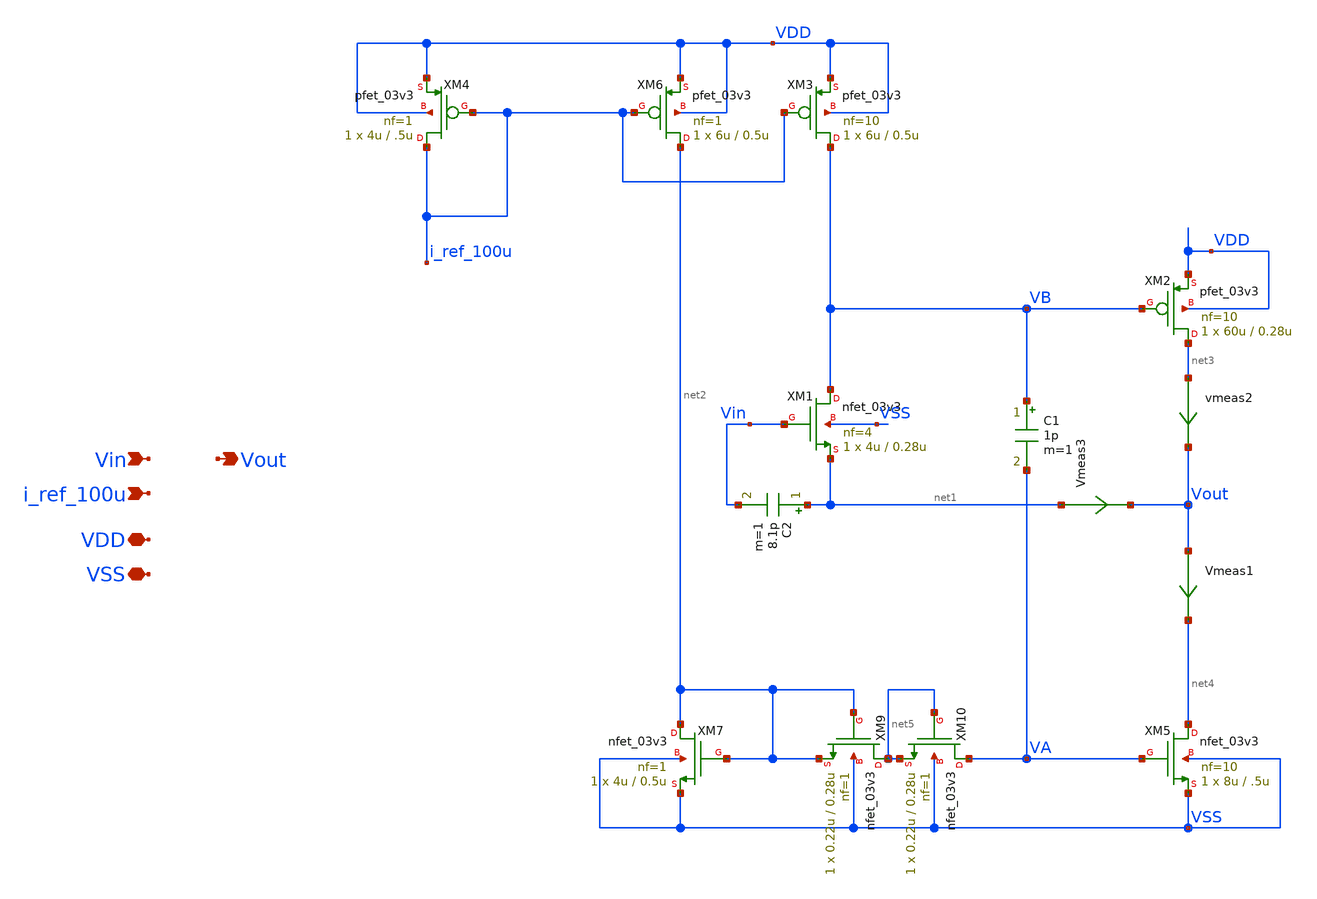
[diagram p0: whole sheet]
** sch_path: designs/output_buffer/schematic/output_buffer_ideal.sch
**.subckt output_buffer_ideal Vin Vout i_ref_100u VDD VSS
*.ipin Vin
*.opin Vout
*.ipin i_ref_100u
*.iopin VDD
*.iopin VSS
XM1 VB Vin net1 VSS nfet_03v3 L=0.28u W=4u nf=4 ad='int((nf+1)/2) * W/nf * 0.18u' as='int((nf+2)/2) * W/nf * 0.18u'
+ pd='2*int((nf+1)/2) * (W/nf + 0.18u)' ps='2*int((nf+2)/2) * (W/nf + 0.18u)' nrd='0.18u / W' nrs='0.18u / W'
+ sa=0 sb=0 sd=0 m=1
XM2 net3 VB VDD VDD pfet_03v3 L=0.28u W=60u nf=10 ad='int((nf+1)/2) * W/nf * 0.18u' as='int((nf+2)/2) * W/nf * 0.18u'
+ pd='2*int((nf+1)/2) * (W/nf + 0.18u)' ps='2*int((nf+2)/2) * (W/nf + 0.18u)' nrd='0.18u / W' nrs='0.18u / W'
+ sa=0 sb=0 sd=0 m=1
XM3 VB i_ref_100u VDD VDD pfet_03v3 L=0.5u W=6u nf=10 ad='int((nf+1)/2) * W/nf * 0.18u' as='int((nf+2)/2) * W/nf * 0.18u'
+ pd='2*int((nf+1)/2) * (W/nf + 0.18u)' ps='2*int((nf+2)/2) * (W/nf + 0.18u)' nrd='0.18u / W' nrs='0.18u / W'
+ sa=0 sb=0 sd=0 m=1
XM4 i_ref_100u i_ref_100u VDD VDD pfet_03v3 L=.5u W=4u nf=1 ad='int((nf+1)/2) * W/nf * 0.18u' as='int((nf+2)/2) * W/nf * 0.18u'
+ pd='2*int((nf+1)/2) * (W/nf + 0.18u)' ps='2*int((nf+2)/2) * (W/nf + 0.18u)' nrd='0.18u / W' nrs='0.18u / W'
+ sa=0 sb=0 sd=0 m=1
XM5 net4 VA VSS VSS nfet_03v3 L=.5u W=8u nf=10 ad='int((nf+1)/2) * W/nf * 0.18u' as='int((nf+2)/2) * W/nf * 0.18u'
+ pd='2*int((nf+1)/2) * (W/nf + 0.18u)' ps='2*int((nf+2)/2) * (W/nf + 0.18u)' nrd='0.18u / W' nrs='0.18u / W'
+ sa=0 sb=0 sd=0 m=1
vmeas2 net3 Vout 0
.save i(vmeas2)
Vmeas1 Vout net4 0
.save i(vmeas1)
C1 VB VA 1p m=1
XM6 net2 i_ref_100u VDD VDD pfet_03v3 L=0.5u W=6u nf=1 ad='int((nf+1)/2) * W/nf * 0.18u' as='int((nf+2)/2) * W/nf * 0.18u'
+ pd='2*int((nf+1)/2) * (W/nf + 0.18u)' ps='2*int((nf+2)/2) * (W/nf + 0.18u)' nrd='0.18u / W' nrs='0.18u / W'
+ sa=0 sb=0 sd=0 m=1
XM7 net2 net2 VSS VSS nfet_03v3 L=0.5u W=4u nf=1 ad='int((nf+1)/2) * W/nf * 0.18u' as='int((nf+2)/2) * W/nf * 0.18u'
+ pd='2*int((nf+1)/2) * (W/nf + 0.18u)' ps='2*int((nf+2)/2) * (W/nf + 0.18u)' nrd='0.18u / W' nrs='0.18u / W'
+ sa=0 sb=0 sd=0 m=1
Vmeas3 net1 Vout 0
.save i(vmeas3)
XM9 net5 net2 net2 VSS nfet_03v3 L=0.28u W=0.22u nf=1 ad='int((nf+1)/2) * W/nf * 0.18u' as='int((nf+2)/2) * W/nf * 0.18u'
+ pd='2*int((nf+1)/2) * (W/nf + 0.18u)' ps='2*int((nf+2)/2) * (W/nf + 0.18u)' nrd='0.18u / W' nrs='0.18u / W'
+ sa=0 sb=0 sd=0 m=1
XM10 VA net5 net5 VSS nfet_03v3 L=0.28u W=0.22u nf=1 ad='int((nf+1)/2) * W/nf * 0.18u' as='int((nf+2)/2) * W/nf * 0.18u'
+ pd='2*int((nf+1)/2) * (W/nf + 0.18u)' ps='2*int((nf+2)/2) * (W/nf + 0.18u)' nrd='0.18u / W' nrs='0.18u / W'
+ sa=0 sb=0 sd=0 m=1
C2 net1 Vin 8.1p m=1
**.ends
.end
